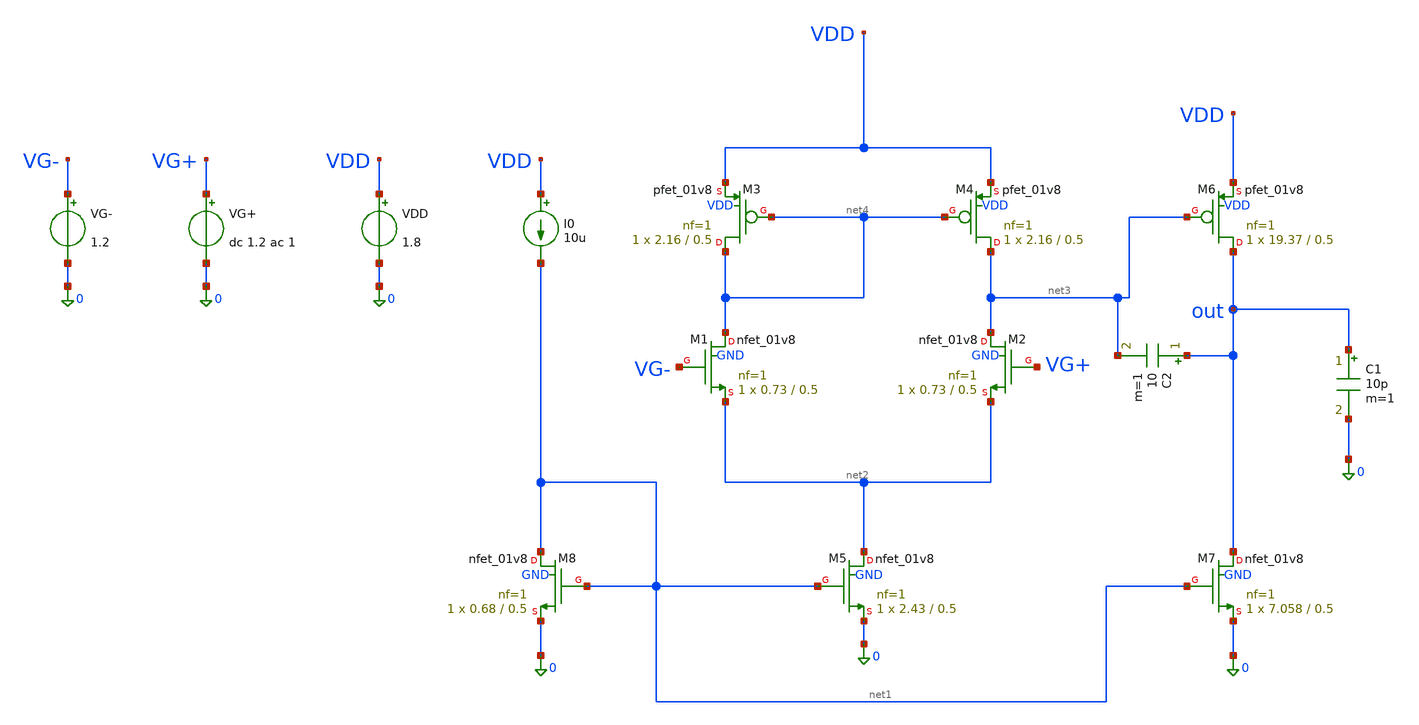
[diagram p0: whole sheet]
** sch_path: schematics/opamp_dc.sch
**.subckt opamp_dc
XM1 net4 VG- net2 GND sky130_fd_pr__nfet_01v8 L=0.5 W=0.73 nf=1 ad='int((1 + 1)/2) * 0.73 / 1 * 0.29'
+ as='int((1 + 2)/2) * 0.73 / 1 * 0.29' pd='2*int((1 + 1)/2) * (0.73 / 1 + 0.29)' ps='2*int((1 + 2)/2) * (0.73 / 1 + 0.29)'
+ nrd='0.29 / 0.73 ' nrs='0.29 / 0.73 ' sa=0 sb=0 sd=0 mult=1 m=1
XM2 net3 VG+ net2 GND sky130_fd_pr__nfet_01v8 L=0.5 W=0.73 nf=1 ad='int((1 + 1)/2) * 0.73 / 1 * 0.29'
+ as='int((1 + 2)/2) * 0.73 / 1 * 0.29' pd='2*int((1 + 1)/2) * (0.73 / 1 + 0.29)' ps='2*int((1 + 2)/2) * (0.73 / 1 + 0.29)'
+ nrd='0.29 / 0.73 ' nrs='0.29 / 0.73 ' sa=0 sb=0 sd=0 mult=1 m=1
XM3 net4 net4 VDD VDD sky130_fd_pr__pfet_01v8 L=0.5 W=2.16 nf=1 ad='int((1 + 1)/2) * 2.16 / 1 * 0.29'
+ as='int((1 + 2)/2) * 2.16 / 1 * 0.29' pd='2*int((1 + 1)/2) * (2.16 / 1 + 0.29)' ps='2*int((1 + 2)/2) * (2.16 / 1 + 0.29)'
+ nrd='0.29 / 2.16 ' nrs='0.29 / 2.16 ' sa=0 sb=0 sd=0 mult=1 m=1
XM4 net3 net4 VDD VDD sky130_fd_pr__pfet_01v8 L=0.5 W=2.16 nf=1 ad='int((1 + 1)/2) * 2.16 / 1 * 0.29'
+ as='int((1 + 2)/2) * 2.16 / 1 * 0.29' pd='2*int((1 + 1)/2) * (2.16 / 1 + 0.29)' ps='2*int((1 + 2)/2) * (2.16 / 1 + 0.29)'
+ nrd='0.29 / 2.16 ' nrs='0.29 / 2.16 ' sa=0 sb=0 sd=0 mult=1 m=1
XM5 net2 net1 0 GND sky130_fd_pr__nfet_01v8 L=0.5 W=2.43 nf=1 ad='int((1 + 1)/2) * 2.43 / 1 * 0.29' as='int((1 + 2)/2) * 2.43 / 1 * 0.29'
+ pd='2*int((1 + 1)/2) * (2.43 / 1 + 0.29)' ps='2*int((1 + 2)/2) * (2.43 / 1 + 0.29)' nrd='0.29 / 2.43 '
+ nrs='0.29 / 2.43 ' sa=0 sb=0 sd=0 mult=1 m=1
XM7 out net1 0 GND sky130_fd_pr__nfet_01v8 L=0.5 W=7.058 nf=1 ad='int((1 + 1)/2) * 7.058 / 1 * 0.29'
+ as='int((1 + 2)/2) * 7.058 / 1 * 0.29' pd='2*int((1 + 1)/2) * (7.058 / 1 + 0.29)' ps='2*int((1 + 2)/2) * (7.058 / 1 + 0.29)'
+ nrd='0.29 / 7.058 ' nrs='0.29 / 7.058 ' sa=0 sb=0 sd=0 mult=1 m=1
XM8 net1 net1 0 GND sky130_fd_pr__nfet_01v8 L=0.5 W=0.68 nf=1 ad='int((1 + 1)/2) * 0.68 / 1 * 0.29' as='int((1 + 2)/2) * 0.68 / 1 * 0.29'
+ pd='2*int((1 + 1)/2) * (0.68 / 1 + 0.29)' ps='2*int((1 + 2)/2) * (0.68 / 1 + 0.29)' nrd='0.29 / 0.68 '
+ nrs='0.29 / 0.68 ' sa=0 sb=0 sd=0 mult=1 m=1
VDD VDD 0 1.8
XM6 out net3 VDD VDD sky130_fd_pr__pfet_01v8 L=0.5 W=19.37 nf=1 ad='int((1 + 1)/2) * 19.37 / 1 * 0.29'
+ as='int((1 + 2)/2) * 19.37 / 1 * 0.29' pd='2*int((1 + 1)/2) * (19.37 / 1 + 0.29)' ps='2*int((1 + 2)/2) * (19.37 / 1 + 0.29)'
+ nrd='0.29 / 19.37 ' nrs='0.29 / 19.37 ' sa=0 sb=0 sd=0 mult=1 m=1
VG+ VG+ 0 dc 1.2 ac 1
I0 VDD net1 10u
VG- VG- 0 1.2
C1 out 0 10p m=1
C2 out net3 10 m=1
**** begin user architecture code

.lib /usr/local/share/pdk/sky130A/libs.tech/ngspice/sky130.lib.spice tt

.control
ac dec 20 1 1G

* Tạo biến cho Biên độ và Pha để file xuất ra gọn gàng
let gain_db = vdb(out)
let phase_deg = cph(v(out))*180/pi

* Vẽ đồ thị trên Ngspice (nếu vẫn muốn xem nhanh)
plot gain_db phase_deg

* Xuất dữ liệu ra file text
wrdata ac_results.txt gain_db phase_deg
.endc

**** end user architecture code
**.ends
.end
